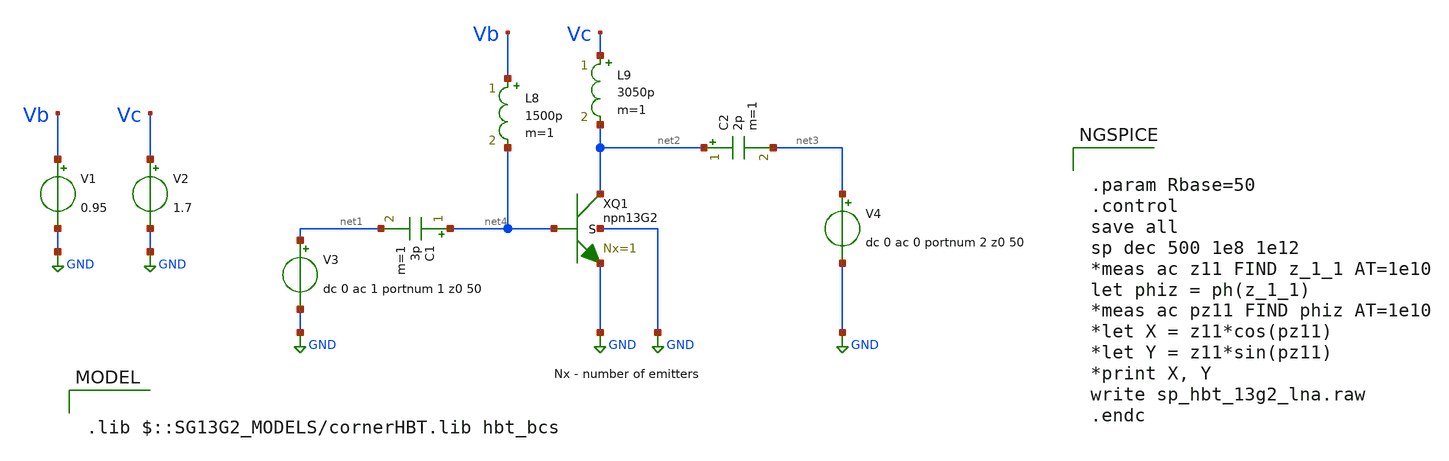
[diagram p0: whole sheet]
** sch_path: ihp-sg13g2/libs.tech/xschem/sg13g2_tests/sp_hbt_13g2_lna2.sch
* Copyright 2023 IHP PDK Authors
**.subckt sp_hbt_13g2_lna2
V4 net3 GND dc 0 ac 0 portnum 2 z0 50
XQ1 net2 net4 GND GND npn13G2 Nx=1
V3 net1 GND dc 0 ac 1 portnum 1 z0 50
V1 Vb GND 0.95
V2 Vc GND 1.7
C1 net4 net1 3p m=1
C2 net2 net3 2p m=1
L8 Vb net4 1500p m=1
L9 Vc net2 3050p m=1
**** begin user architecture code

.lib $::SG13G2_MODELS/cornerHBT.lib hbt_bcs



.param Rbase=50
.control
save all
sp dec 500 1e8 1e12
*meas ac z11 FIND z_1_1 AT=1e10
let phiz = ph(z_1_1)
*meas ac pz11 FIND phiz AT=1e10
*let X = z11*cos(pz11)
*let Y = z11*sin(pz11)
*print X, Y
write sp_hbt_13g2_lna.raw
.endc


**** end user architecture code
**.ends
.GLOBAL GND
.end
